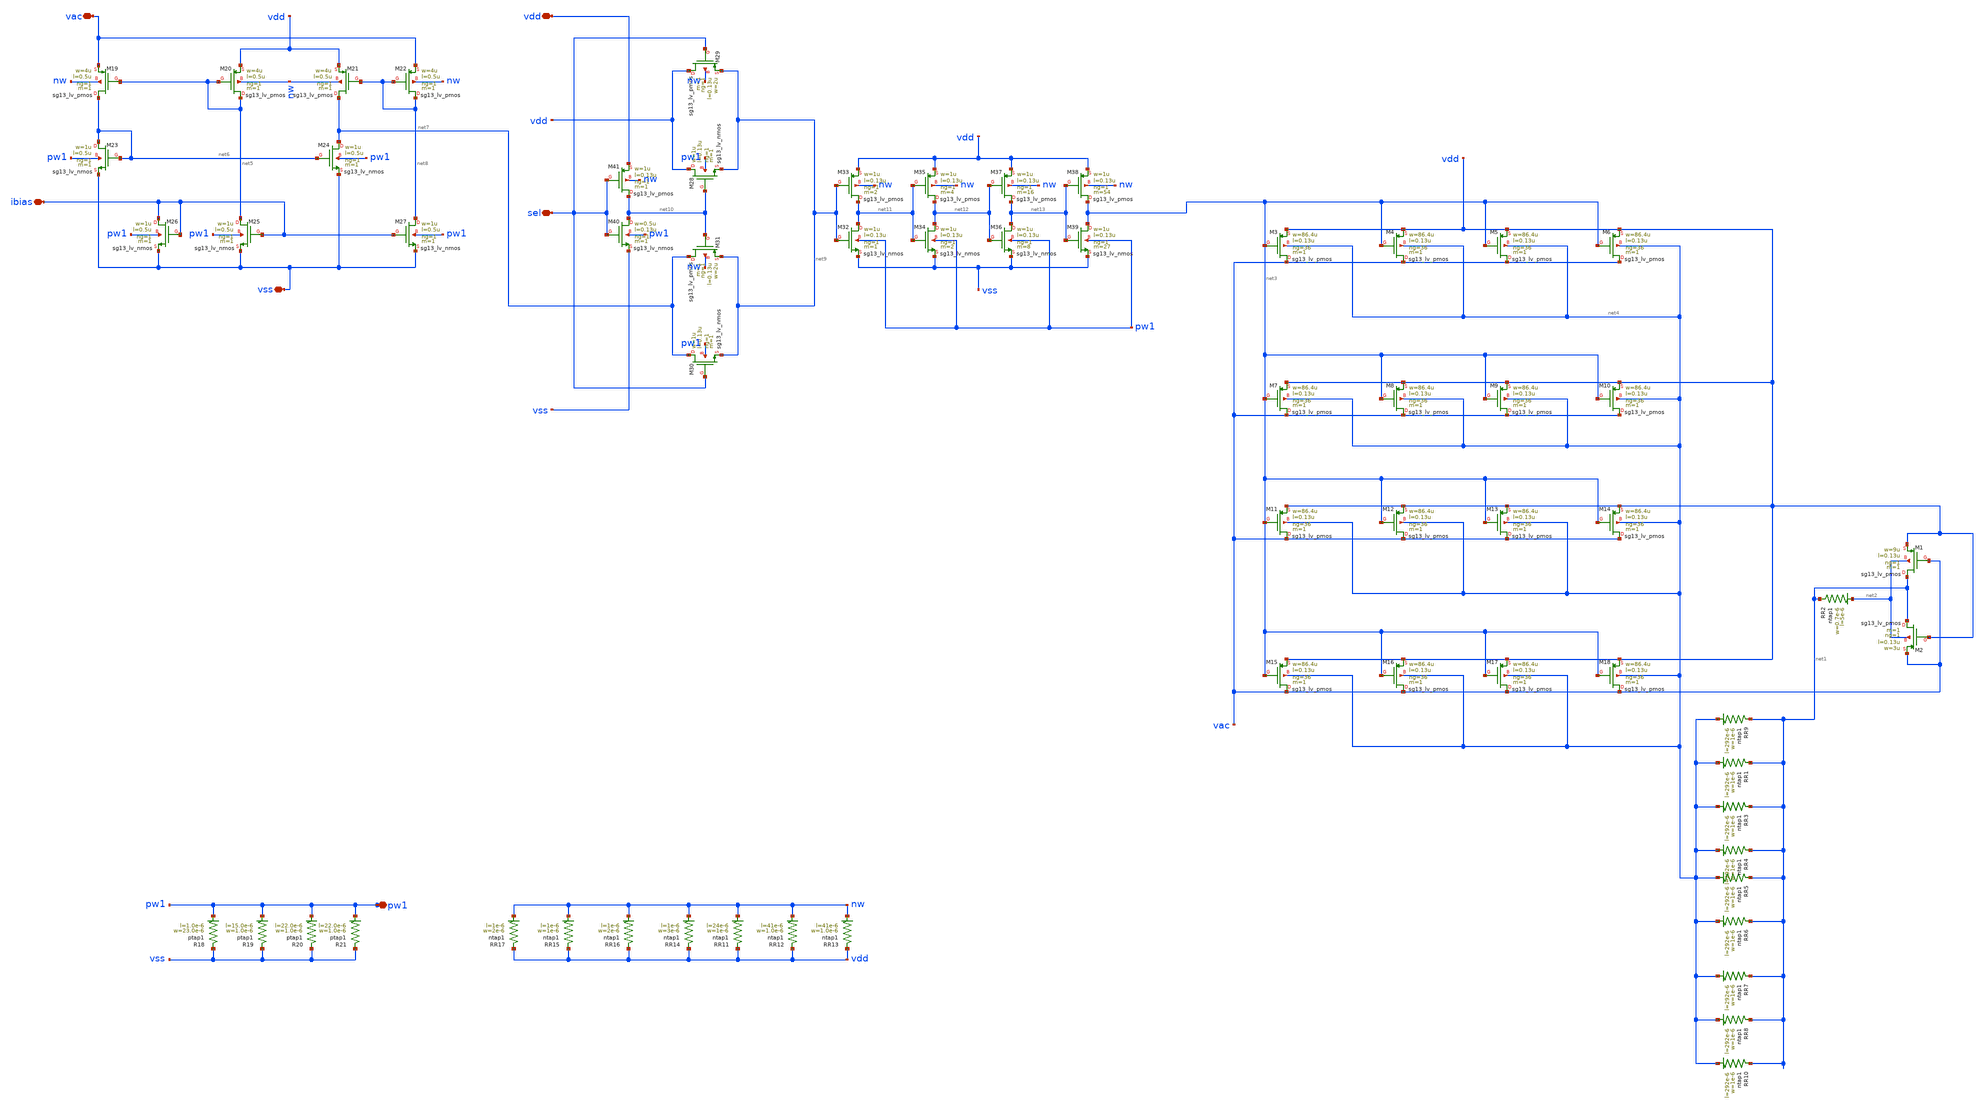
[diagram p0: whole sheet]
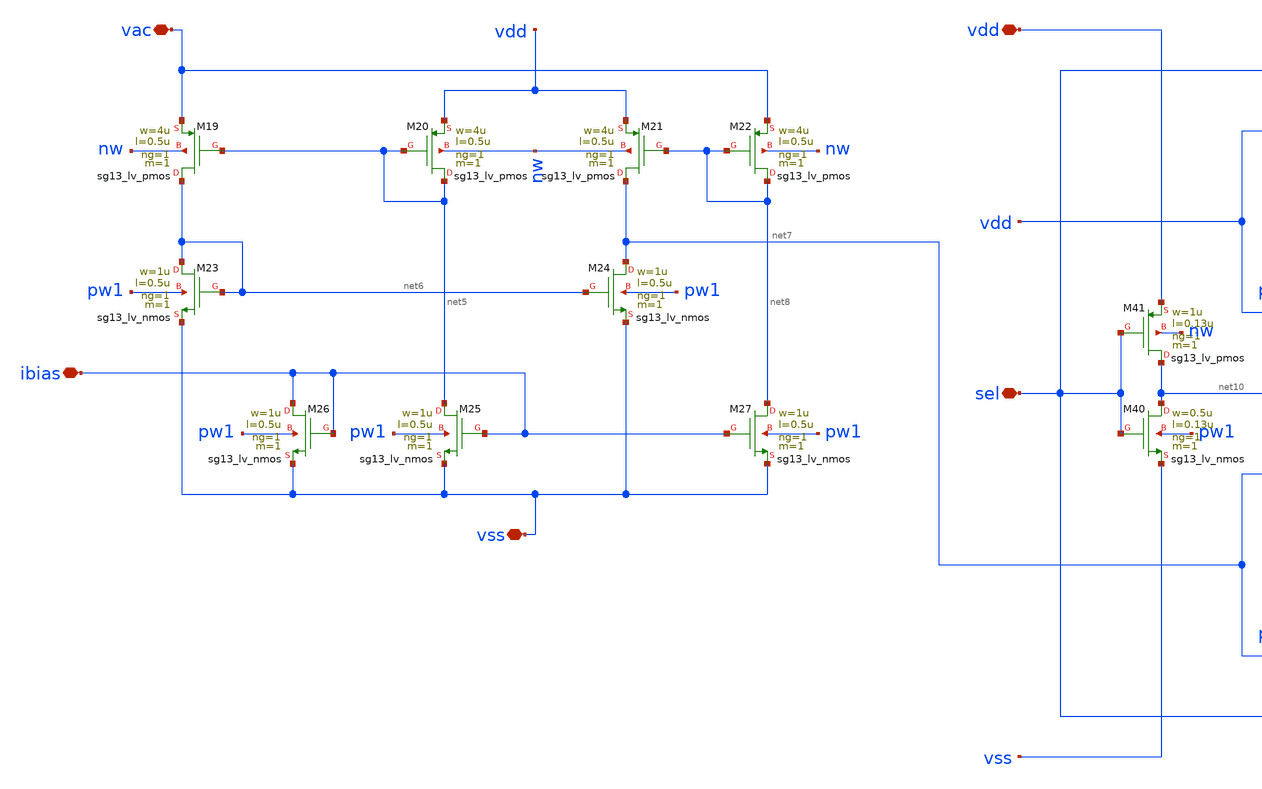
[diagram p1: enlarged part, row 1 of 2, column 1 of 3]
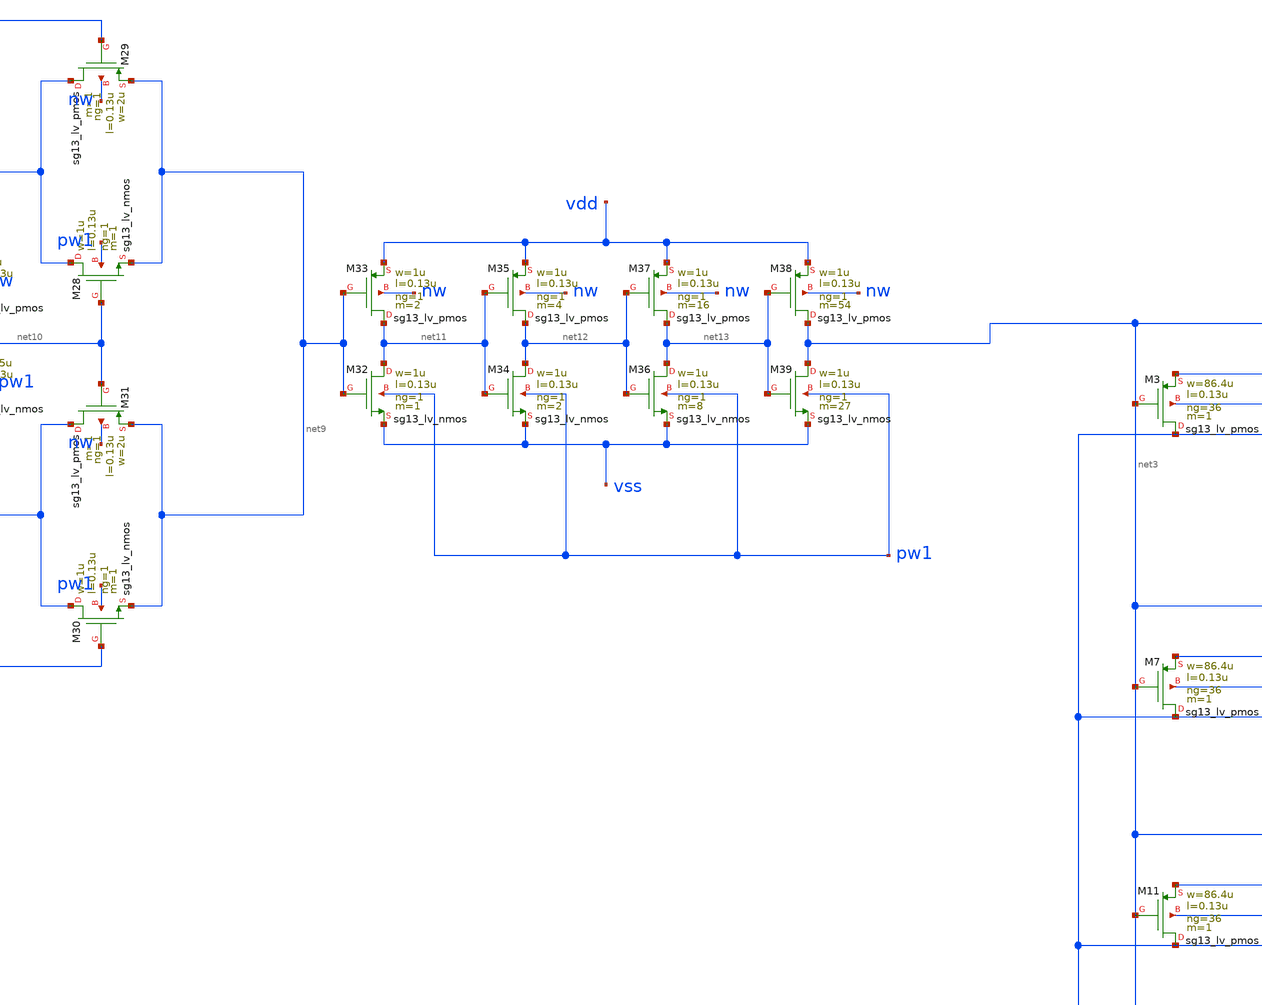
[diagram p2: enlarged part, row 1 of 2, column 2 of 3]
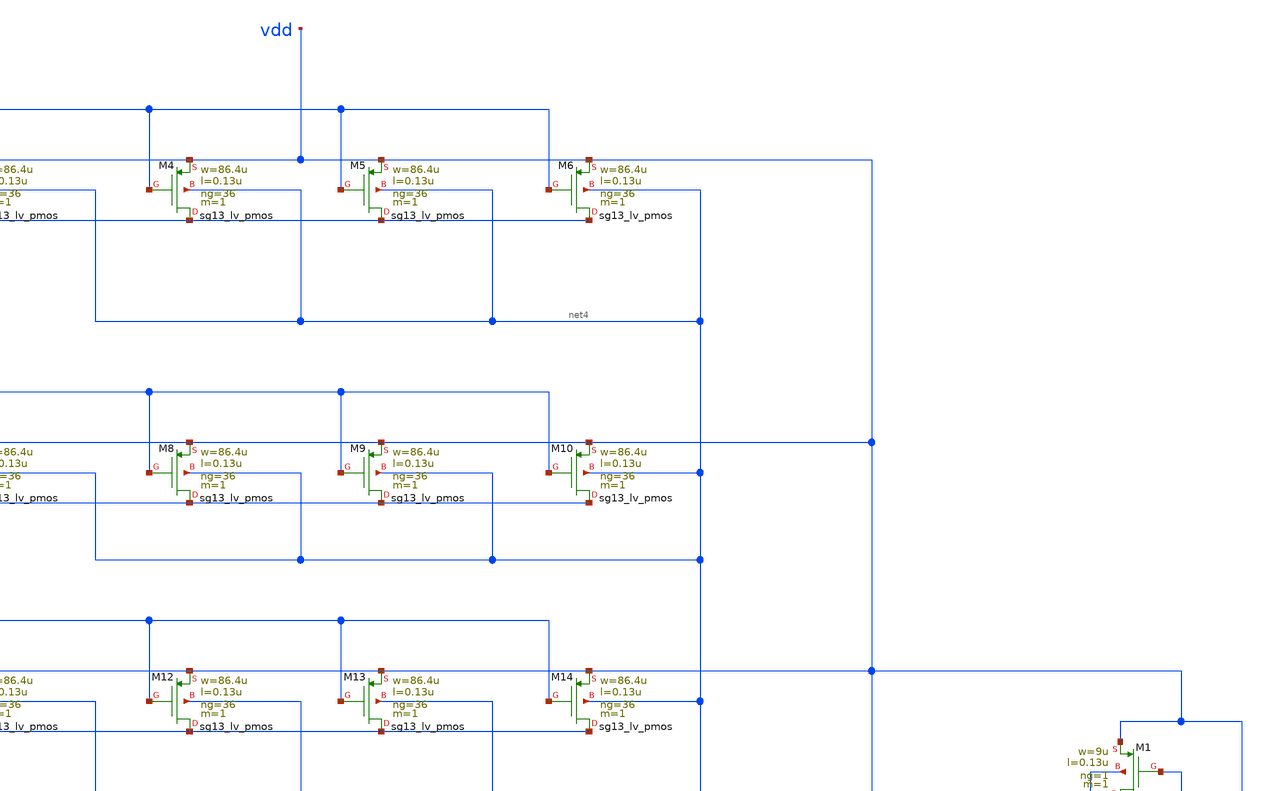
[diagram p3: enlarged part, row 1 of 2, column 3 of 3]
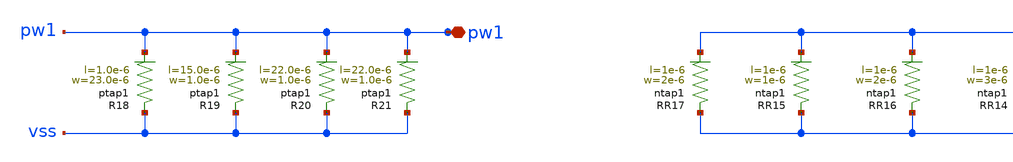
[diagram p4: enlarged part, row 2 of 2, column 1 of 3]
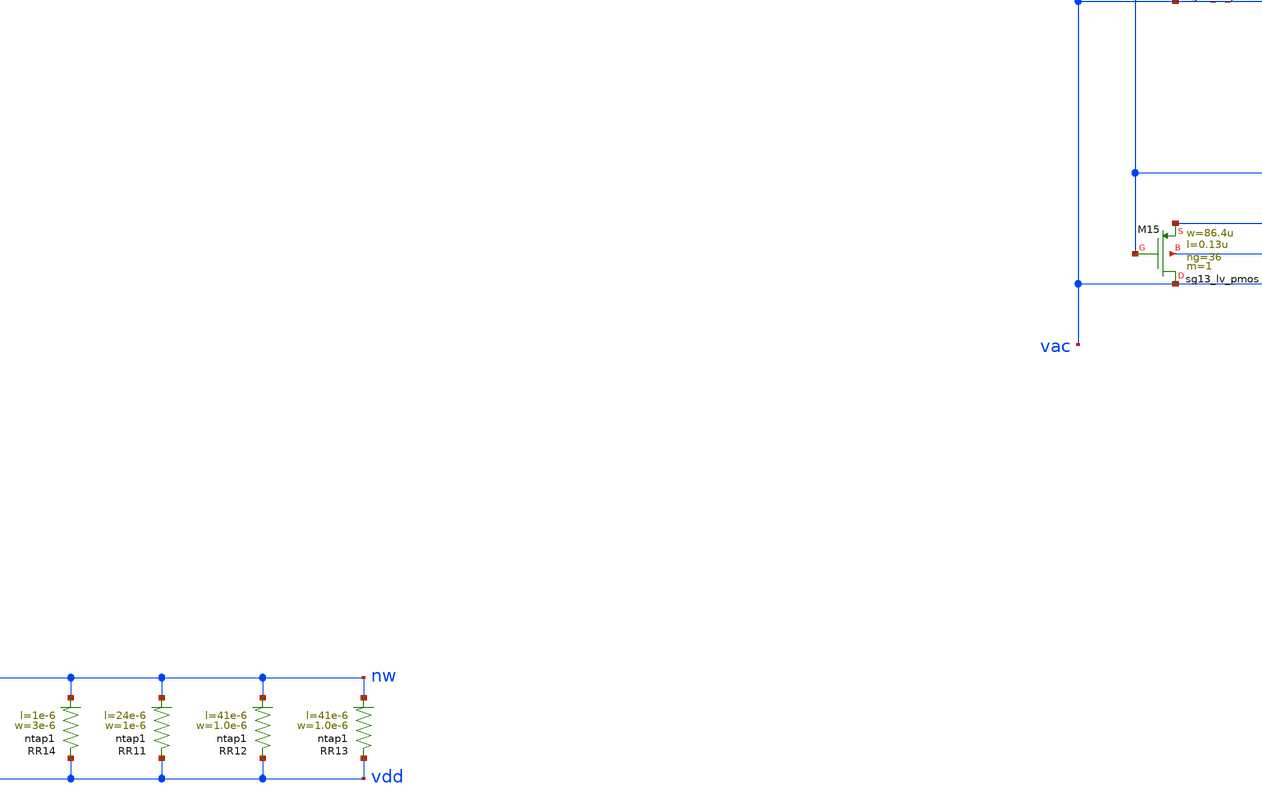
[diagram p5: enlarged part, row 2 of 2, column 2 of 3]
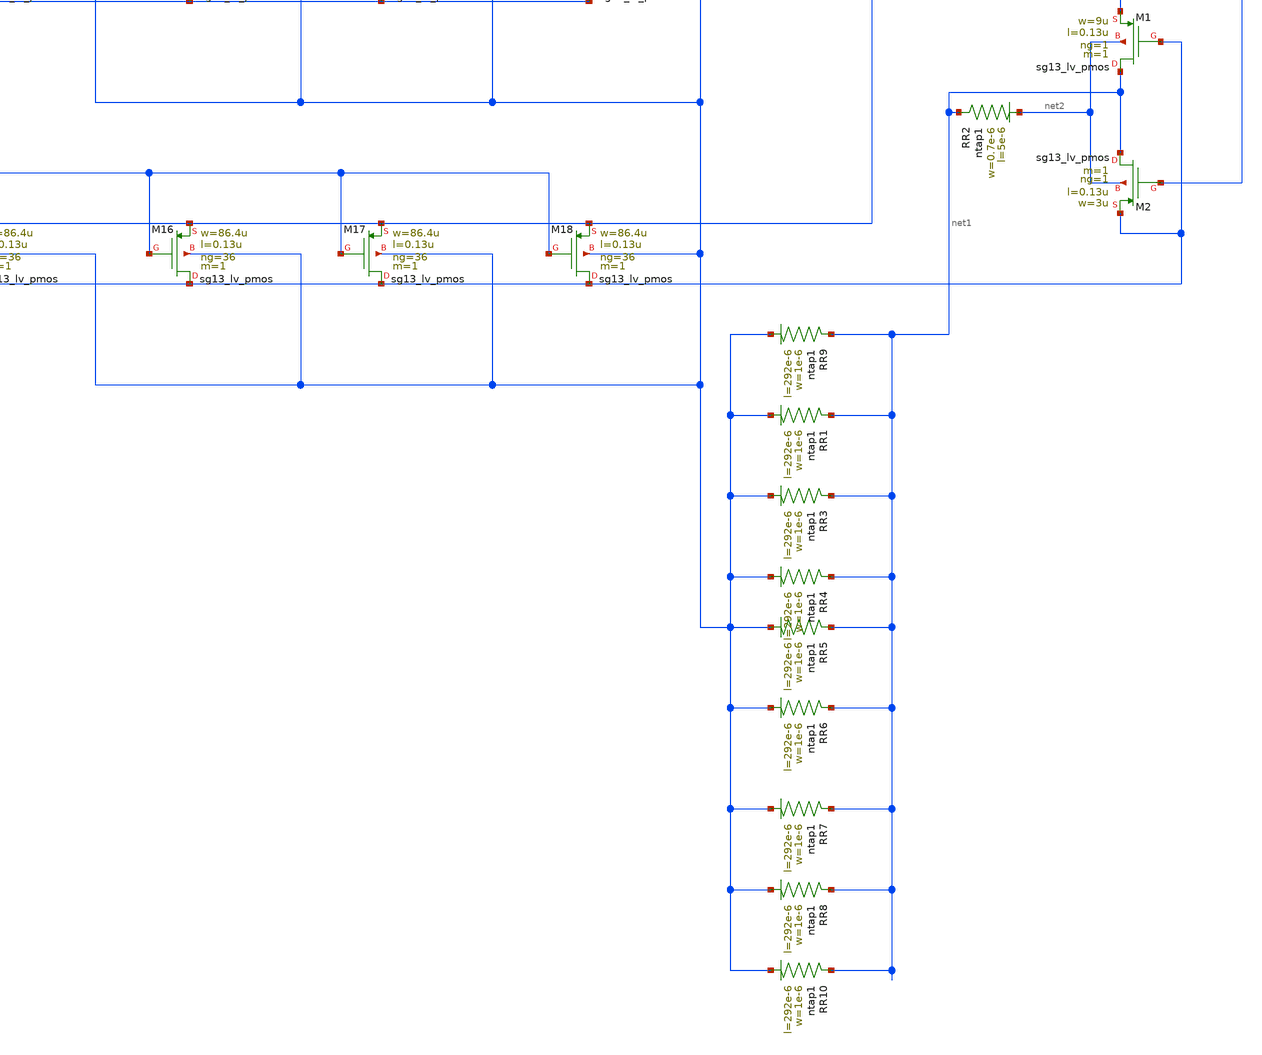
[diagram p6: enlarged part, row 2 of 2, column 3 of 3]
** sch_path: Layouts/PMOS/PMOS_w_bodybias_w_driver.sch
**.subckt PMOS_w_bodybias_w_driver vdd ibias vac vss sel pw1
*.iopin vdd
*.iopin ibias
*.iopin vac
*.iopin vss
*.iopin sel
*.iopin pw1
XM1 net1 vac vdd net2 sg13_lv_pmos w=9u l=0.13u ng=1 m=1 mm_ok=1
XM2 net1 vdd vac net2 sg13_lv_pmos w=3u l=0.13u ng=1 m=1 mm_ok=1
XR2 net1 net2 ntap1 R=65.77 w=0.7e-6 l=5e-6
XM3 vac net3 vdd net4 sg13_lv_pmos w=86.4u l=0.13u ng=36 m=1 mm_ok=1
XM4 vac net3 vdd net4 sg13_lv_pmos w=86.4u l=0.13u ng=36 m=1 mm_ok=1
XM5 vac net3 vdd net4 sg13_lv_pmos w=86.4u l=0.13u ng=36 m=1 mm_ok=1
XM6 vac net3 vdd net4 sg13_lv_pmos w=86.4u l=0.13u ng=36 m=1 mm_ok=1
XM7 vac net3 vdd net4 sg13_lv_pmos w=86.4u l=0.13u ng=36 m=1 mm_ok=1
XM8 vac net3 vdd net4 sg13_lv_pmos w=86.4u l=0.13u ng=36 m=1 mm_ok=1
XM9 vac net3 vdd net4 sg13_lv_pmos w=86.4u l=0.13u ng=36 m=1 mm_ok=1
XM10 vac net3 vdd net4 sg13_lv_pmos w=86.4u l=0.13u ng=36 m=1 mm_ok=1
XM11 vac net3 vdd net4 sg13_lv_pmos w=86.4u l=0.13u ng=36 m=1 mm_ok=1
XM12 vac net3 vdd net4 sg13_lv_pmos w=86.4u l=0.13u ng=36 m=1 mm_ok=1
XM13 vac net3 vdd net4 sg13_lv_pmos w=86.4u l=0.13u ng=36 m=1 mm_ok=1
XM14 vac net3 vdd net4 sg13_lv_pmos w=86.4u l=0.13u ng=36 m=1 mm_ok=1
XM15 vac net3 vdd net4 sg13_lv_pmos w=86.4u l=0.13u ng=36 m=1 mm_ok=1
XM16 vac net3 vdd net4 sg13_lv_pmos w=86.4u l=0.13u ng=36 m=1 mm_ok=1
XM17 vac net3 vdd net4 sg13_lv_pmos w=86.4u l=0.13u ng=36 m=1 mm_ok=1
XM18 vac net3 vdd net4 sg13_lv_pmos w=86.4u l=0.13u ng=36 m=1 mm_ok=1
XR9 net1 net4 ntap1 R=1.116 w=1e-6 l=292e-6
XR1 net1 net4 ntap1 R=1.116 w=1e-6 l=292e-6
XR3 net1 net4 ntap1 R=1.116 w=1e-6 l=292e-6
XR4 net1 net4 ntap1 R=1.116 w=1e-6 l=292e-6
XR5 net1 net4 ntap1 R=1.116 w=1e-6 l=292e-6
XR6 net1 net4 ntap1 R=1.116 w=1e-6 l=292e-6
XR7 net1 net4 ntap1 R=1.116 w=1e-6 l=292e-6
XR8 net1 net4 ntap1 R=1.116 w=1e-6 l=292e-6
XR10 net1 net4 ntap1 R=1.116 w=1e-6 l=292e-6
XM19 net6 net5 vac nw sg13_lv_pmos w=4u l=0.5u ng=1 m=1 mm_ok=1
XM20 net5 net5 vdd nw sg13_lv_pmos w=4u l=0.5u ng=1 m=1 mm_ok=1
XM21 net7 net8 vdd nw sg13_lv_pmos w=4u l=0.5u ng=1 m=1 mm_ok=1
XM22 net8 net8 vac nw sg13_lv_pmos w=4u l=0.5u ng=1 m=1 mm_ok=1
XM23 net6 net6 vss pw1 sg13_lv_nmos w=1u l=0.5u ng=1 m=1 mm_ok=1
XM24 net7 net6 vss pw1 sg13_lv_nmos w=1u l=0.5u ng=1 m=1 mm_ok=1
XM25 net5 ibias vss pw1 sg13_lv_nmos w=1u l=0.5u ng=1 m=1 mm_ok=1
XM26 ibias ibias vss pw1 sg13_lv_nmos w=1u l=0.5u ng=1 m=1 mm_ok=1
XM27 net8 ibias vss pw1 sg13_lv_nmos w=1u l=0.5u ng=1 m=1 mm_ok=1
XR11 vdd nw ntap1 R=13.24 w=1e-6 l=24e-6
XR12 vdd nw ntap1 R=7.84 w=1.0e-6 l=41e-6
XR13 vdd nw ntap1 R=7.84 w=1.0e-6 l=41e-6
XM28 vdd net10 net9 pw1 sg13_lv_nmos w=1u l=0.13u ng=1 m=1 mm_ok=1
XM29 vdd sel net9 nw sg13_lv_pmos w=2u l=0.13u ng=1 m=1 mm_ok=1
XM30 net7 sel net9 pw1 sg13_lv_nmos w=1u l=0.13u ng=1 m=1 mm_ok=1
XM31 net7 net10 net9 nw sg13_lv_pmos w=2u l=0.13u ng=1 m=1 mm_ok=1
XM32 net11 net9 vss pw1 sg13_lv_nmos w=1u l=0.13u ng=1 m=1 mm_ok=1
XM33 net11 net9 vdd nw sg13_lv_pmos w=1u l=0.13u ng=1 m=2 mm_ok=1
XM34 net12 net11 vss pw1 sg13_lv_nmos w=1u l=0.13u ng=1 m=2 mm_ok=1
XM35 net12 net11 vdd nw sg13_lv_pmos w=1u l=0.13u ng=1 m=4 mm_ok=1
XM36 net13 net12 vss pw1 sg13_lv_nmos w=1u l=0.13u ng=1 m=8 mm_ok=1
XM37 net13 net12 vdd nw sg13_lv_pmos w=1u l=0.13u ng=1 m=16 mm_ok=1
XM38 net3 net13 vdd nw sg13_lv_pmos w=1u l=0.13u ng=1 m=54 mm_ok=1
XM39 net3 net13 vss pw1 sg13_lv_nmos w=1u l=0.13u ng=1 m=27 mm_ok=1
XR14 vdd nw ntap1 R=89.09 w=3e-6 l=1e-6
XR15 vdd nw ntap1 R=196 w=1e-6 l=1e-6
XR16 vdd nw ntap1 R=122.5 w=2e-6 l=1e-6
XR17 vdd nw ntap1 R=122.5 w=2e-6 l=1e-6
XR18 vss pw1 ptap1 R=13.8 w=23.0e-6 l=1.0e-6
XR19 vss pw1 ptap1 R=20.85 w=1.0e-6 l=15.0e-6
XR20 vss pw1 ptap1 R=14.41 w=1.0e-6 l=22.0e-6
XR21 vss pw1 ptap1 R=14.41 w=1.0e-6 l=22.0e-6
XM40 net10 sel vss pw1 sg13_lv_nmos w=0.5u l=0.13u ng=1 m=1 mm_ok=1
XM41 net10 sel vdd nw sg13_lv_pmos w=1u l=0.13u ng=1 m=1 mm_ok=1
**.ends
.end
